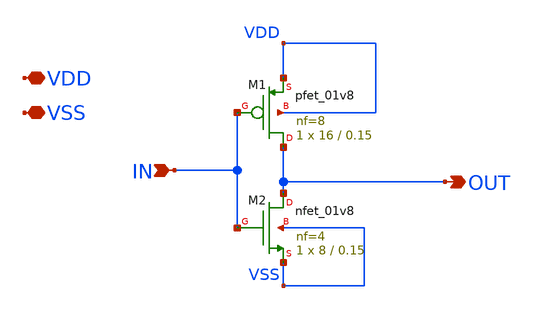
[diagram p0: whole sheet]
** sch_path: xschem/tuning/single_inverter_tune.sch
**.subckt single_inverter_tune VDD VSS IN OUT
*.iopin VDD
*.iopin VSS
*.ipin IN
*.opin OUT
XM1 OUT IN VDD VDD sky130_fd_pr__pfet_01v8 L=0.15 W=16 nf=8 ad='int((nf+1)/2) * W/nf * 0.29' as='int((nf+2)/2) * W/nf * 0.29'
+ pd='2*int((nf+1)/2) * (W/nf + 0.29)' ps='2*int((nf+2)/2) * (W/nf + 0.29)' nrd='0.29 / W' nrs='0.29 / W'
+ sa=0 sb=0 sd=0 mult=1 m=1
XM2 OUT IN VSS VSS sky130_fd_pr__nfet_01v8 L=0.15 W=8 nf=4 ad='int((nf+1)/2) * W/nf * 0.29' as='int((nf+2)/2) * W/nf * 0.29'
+ pd='2*int((nf+1)/2) * (W/nf + 0.29)' ps='2*int((nf+2)/2) * (W/nf + 0.29)' nrd='0.29 / W' nrs='0.29 / W'
+ sa=0 sb=0 sd=0 mult=1 m=1
**.ends
.end
